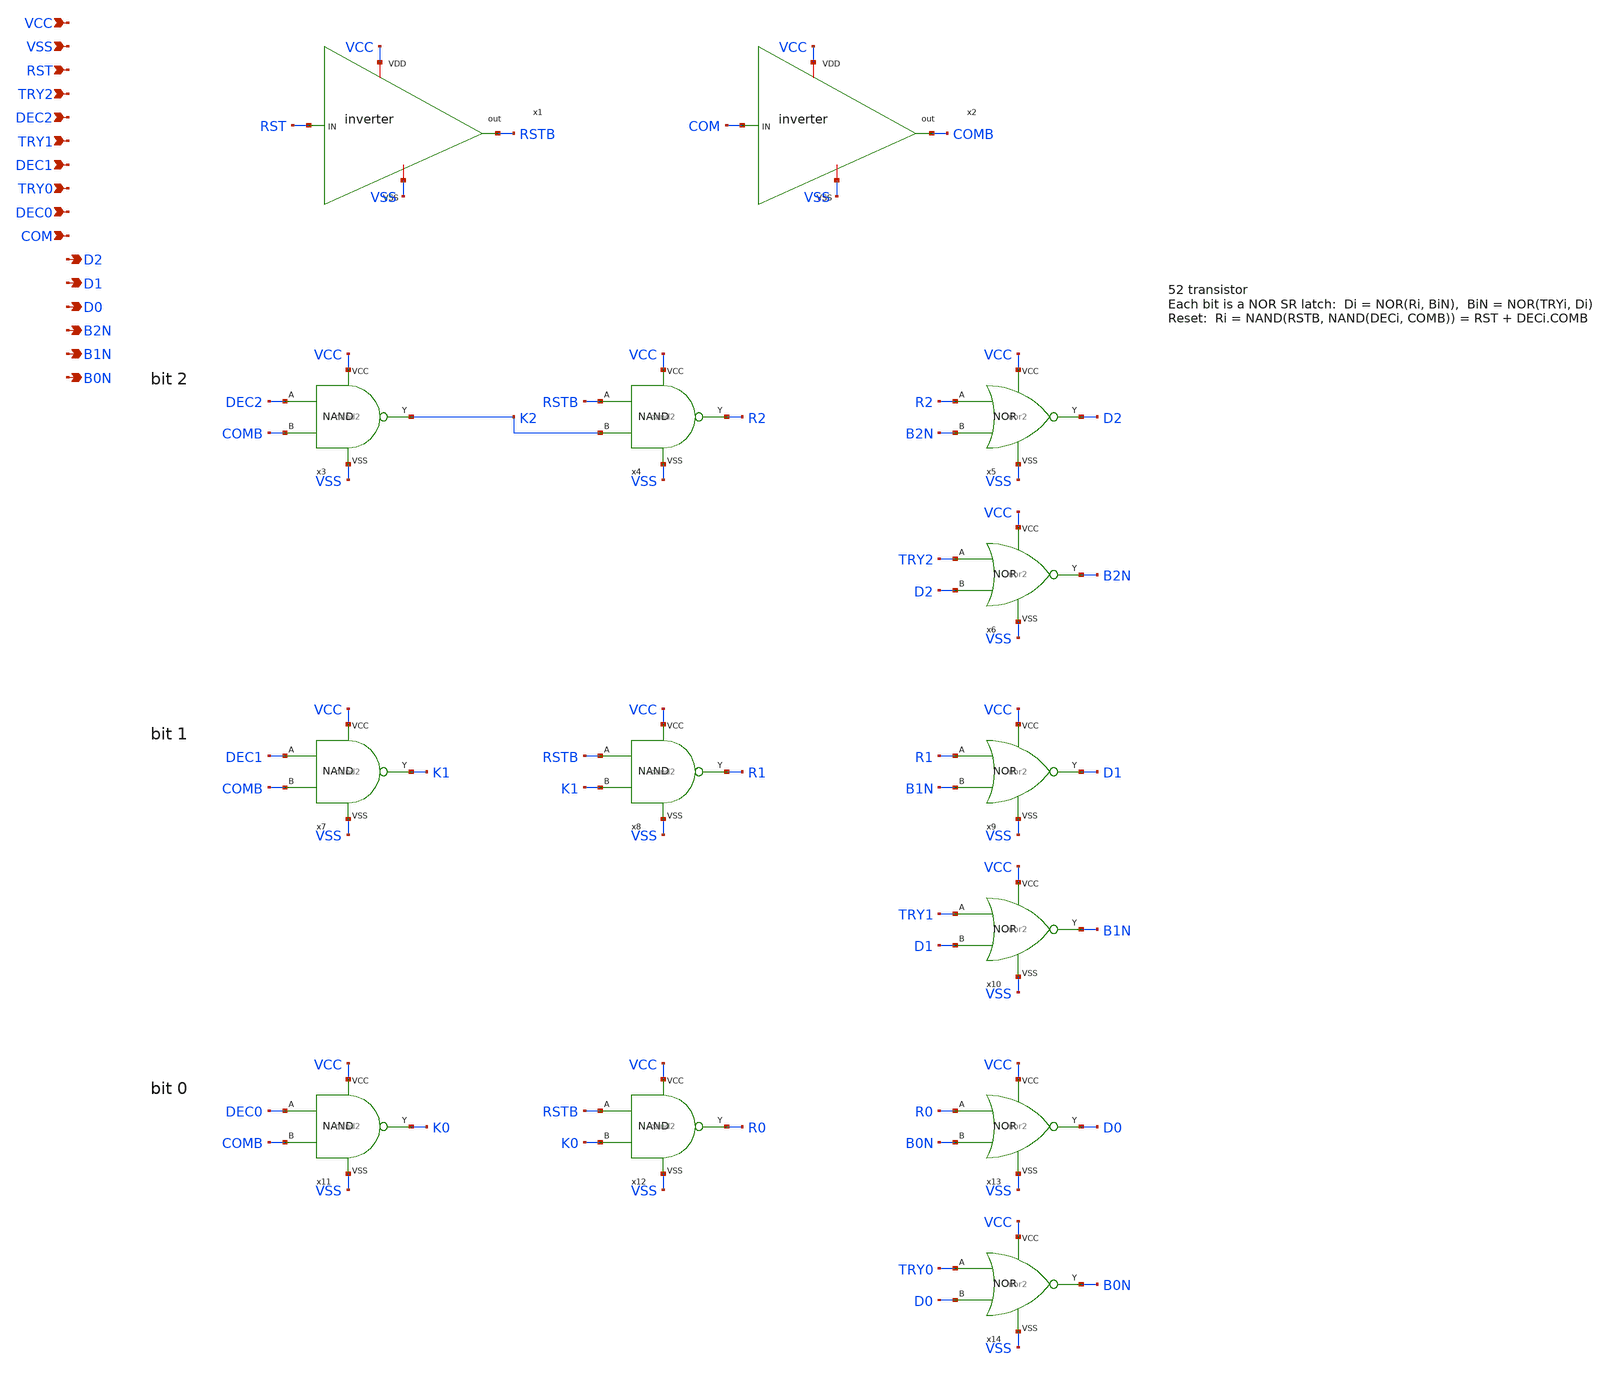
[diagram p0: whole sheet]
** sch_path: sar_logic3_simple.sch
**.subckt sar_logic3_simple VCC VSS RST TRY2 DEC2 TRY1 DEC1 TRY0 DEC0 COM D2 D1 D0 B2N B1N B0N
*.ipin VCC
*.ipin VSS
*.ipin RST
*.ipin TRY2
*.ipin DEC2
*.ipin TRY1
*.ipin DEC1
*.ipin TRY0
*.ipin DEC0
*.ipin COM
*.opin D2
*.opin D1
*.opin D0
*.opin B2N
*.opin B1N
*.opin B0N
x1 VCC RST RSTB VSS inverter
x2 VCC COM COMB VSS inverter
x3 DEC2 COMB K2 VCC VSS nand2
x4 RSTB K2 R2 VCC VSS nand2
x5 R2 B2N D2 VCC VSS nor2
x6 TRY2 D2 B2N VCC VSS nor2
x7 DEC1 COMB K1 VCC VSS nand2
x8 RSTB K1 R1 VCC VSS nand2
x9 R1 B1N D1 VCC VSS nor2
x10 TRY1 D1 B1N VCC VSS nor2
x11 DEC0 COMB K0 VCC VSS nand2
x12 RSTB K0 R0 VCC VSS nand2
x13 R0 B0N D0 VCC VSS nor2
x14 TRY0 D0 B0N VCC VSS nor2
**.ends

* expanding   symbol:  /home/ttuser/Documents/ADCAnalogDesign/inverter.sym # of pins=4
** sym_path: inverter.sym
** sch_path: inverter.sch
.subckt inverter VDD IN out VSS
*.ipin IN
*.opin out
*.iopin VDD
*.iopin VSS
XM3 out IN VDD VDD sky130_fd_pr__pfet_01v8 L=0.15 W=1 nf=1 ad='int((nf+1)/2) * W/nf * 0.29' as='int((nf+2)/2) * W/nf * 0.29'
+ pd='2*int((nf+1)/2) * (W/nf + 0.29)' ps='2*int((nf+2)/2) * (W/nf + 0.29)' nrd='0.29 / W' nrs='0.29 / W'
+ sa=0 sb=0 sd=0 mult=1 m=1
XM2 out IN VSS VSS sky130_fd_pr__nfet_01v8 L=0.15 W=1 nf=1 ad='int((nf+1)/2) * W/nf * 0.29' as='int((nf+2)/2) * W/nf * 0.29'
+ pd='2*int((nf+1)/2) * (W/nf + 0.29)' ps='2*int((nf+2)/2) * (W/nf + 0.29)' nrd='0.29 / W' nrs='0.29 / W'
+ sa=0 sb=0 sd=0 mult=1 m=1
.ends


* expanding   symbol:  /home/ttuser/Documents/ADCAnalogDesign/nand2.sym # of pins=5
** sym_path: nand2.sym
** sch_path: nand2.sch
.subckt nand2 A B Y VCC VSS
*.ipin A
*.ipin B
*.opin Y
*.iopin VCC
*.iopin VSS
XM1 Y A VCC VCC sky130_fd_pr__pfet_01v8 L=0.15 W=2 nf=1 ad='int((nf+1)/2) * W/nf * 0.29' as='int((nf+2)/2) * W/nf * 0.29'
+ pd='2*int((nf+1)/2) * (W/nf + 0.29)' ps='2*int((nf+2)/2) * (W/nf + 0.29)' nrd='0.29 / W' nrs='0.29 / W'
+ sa=0 sb=0 sd=0 mult=1 m=1
XM2 Y B VCC VCC sky130_fd_pr__pfet_01v8 L=0.15 W=2 nf=1 ad='int((nf+1)/2) * W/nf * 0.29' as='int((nf+2)/2) * W/nf * 0.29'
+ pd='2*int((nf+1)/2) * (W/nf + 0.29)' ps='2*int((nf+2)/2) * (W/nf + 0.29)' nrd='0.29 / W' nrs='0.29 / W'
+ sa=0 sb=0 sd=0 mult=1 m=1
XM3 Y A N1 VSS sky130_fd_pr__nfet_01v8 L=0.15 W=2 nf=1 ad='int((nf+1)/2) * W/nf * 0.29' as='int((nf+2)/2) * W/nf * 0.29'
+ pd='2*int((nf+1)/2) * (W/nf + 0.29)' ps='2*int((nf+2)/2) * (W/nf + 0.29)' nrd='0.29 / W' nrs='0.29 / W'
+ sa=0 sb=0 sd=0 mult=1 m=1
XM4 N1 B VSS VSS sky130_fd_pr__nfet_01v8 L=0.15 W=2 nf=1 ad='int((nf+1)/2) * W/nf * 0.29' as='int((nf+2)/2) * W/nf * 0.29'
+ pd='2*int((nf+1)/2) * (W/nf + 0.29)' ps='2*int((nf+2)/2) * (W/nf + 0.29)' nrd='0.29 / W' nrs='0.29 / W'
+ sa=0 sb=0 sd=0 mult=1 m=1
.ends


* expanding   symbol:  /home/ttuser/Documents/ADCAnalogDesign/nor2.sym # of pins=5
** sym_path: nor2.sym
** sch_path: nor2.sch
.subckt nor2 A B Y VCC VSS
*.ipin A
*.ipin B
*.opin Y
*.iopin VCC
*.iopin VSS
XM1 P1 A VCC VCC sky130_fd_pr__pfet_01v8 L=0.15 W=4 nf=1 ad='int((nf+1)/2) * W/nf * 0.29' as='int((nf+2)/2) * W/nf * 0.29'
+ pd='2*int((nf+1)/2) * (W/nf + 0.29)' ps='2*int((nf+2)/2) * (W/nf + 0.29)' nrd='0.29 / W' nrs='0.29 / W'
+ sa=0 sb=0 sd=0 mult=1 m=1
XM2 Y B P1 VCC sky130_fd_pr__pfet_01v8 L=0.15 W=4 nf=1 ad='int((nf+1)/2) * W/nf * 0.29' as='int((nf+2)/2) * W/nf * 0.29'
+ pd='2*int((nf+1)/2) * (W/nf + 0.29)' ps='2*int((nf+2)/2) * (W/nf + 0.29)' nrd='0.29 / W' nrs='0.29 / W'
+ sa=0 sb=0 sd=0 mult=1 m=1
XM3 Y A VSS VSS sky130_fd_pr__nfet_01v8 L=0.15 W=1 nf=1 ad='int((nf+1)/2) * W/nf * 0.29' as='int((nf+2)/2) * W/nf * 0.29'
+ pd='2*int((nf+1)/2) * (W/nf + 0.29)' ps='2*int((nf+2)/2) * (W/nf + 0.29)' nrd='0.29 / W' nrs='0.29 / W'
+ sa=0 sb=0 sd=0 mult=1 m=1
XM4 Y B VSS VSS sky130_fd_pr__nfet_01v8 L=0.15 W=1 nf=1 ad='int((nf+1)/2) * W/nf * 0.29' as='int((nf+2)/2) * W/nf * 0.29'
+ pd='2*int((nf+1)/2) * (W/nf + 0.29)' ps='2*int((nf+2)/2) * (W/nf + 0.29)' nrd='0.29 / W' nrs='0.29 / W'
+ sa=0 sb=0 sd=0 mult=1 m=1
.ends

.end
